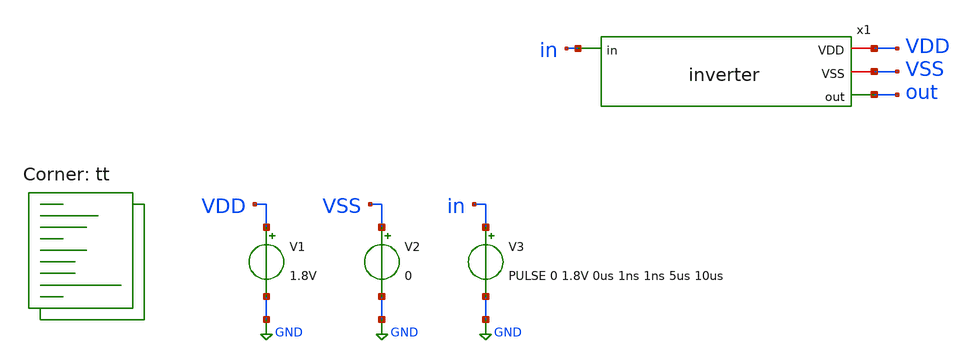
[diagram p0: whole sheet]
** sch_path: xschem/tests/inverter_test.sch
**.subckt inverter_test
x1 VDD VSS out in inverter
V1 VDD GND 1.8V
V2 VSS GND 0
V3 in GND PULSE 0 1.8V 0us 1ns 1ns 5us 10us
**** begin user architecture code
.lib $::SKYWATER_MODELS/sky130.lib.spice tt
 *.lib $::SKYWATER_MODELS/sky130.lib.spice tt
.include $::SKYWATER_STDCELLS/sky130_fd_sc_hd.spice




* ngspice commands
.options list act
.options method=gear
.temp 25

.control
save all
tran 0.1 40u

write inverter_test.raw
.endc




**** end user architecture code
**.ends

* expanding   symbol:  src/inverter.sym # of pins=4
** sym_path: xschem/src/inverter.sym
** sch_path: xschem/src/inverter.sch
.subckt inverter VDD VSS out in
*.ipin in
*.opin out
*.iopin VSS
*.iopin VDD
XM1 out in VSS VSS sky130_fd_pr__nfet_01v8 L=0.15 W=1 nf=1 ad='int((nf+1)/2) * W/nf * 0.29' as='int((nf+2)/2) * W/nf * 0.29'
+ pd='2*int((nf+1)/2) * (W/nf + 0.29)' ps='2*int((nf+2)/2) * (W/nf + 0.29)' nrd='0.29 / W' nrs='0.29 / W'
+ sa=0 sb=0 sd=0 mult=1 m=1
XM2 out in VDD VDD sky130_fd_pr__pfet_01v8 L=0.15 W=1.76 nf=1 ad='int((nf+1)/2) * W/nf * 0.29' as='int((nf+2)/2) * W/nf * 0.29'
+ pd='2*int((nf+1)/2) * (W/nf + 0.29)' ps='2*int((nf+2)/2) * (W/nf + 0.29)' nrd='0.29 / W' nrs='0.29 / W'
+ sa=0 sb=0 sd=0 mult=1 m=1
.ends

.GLOBAL GND
.end
